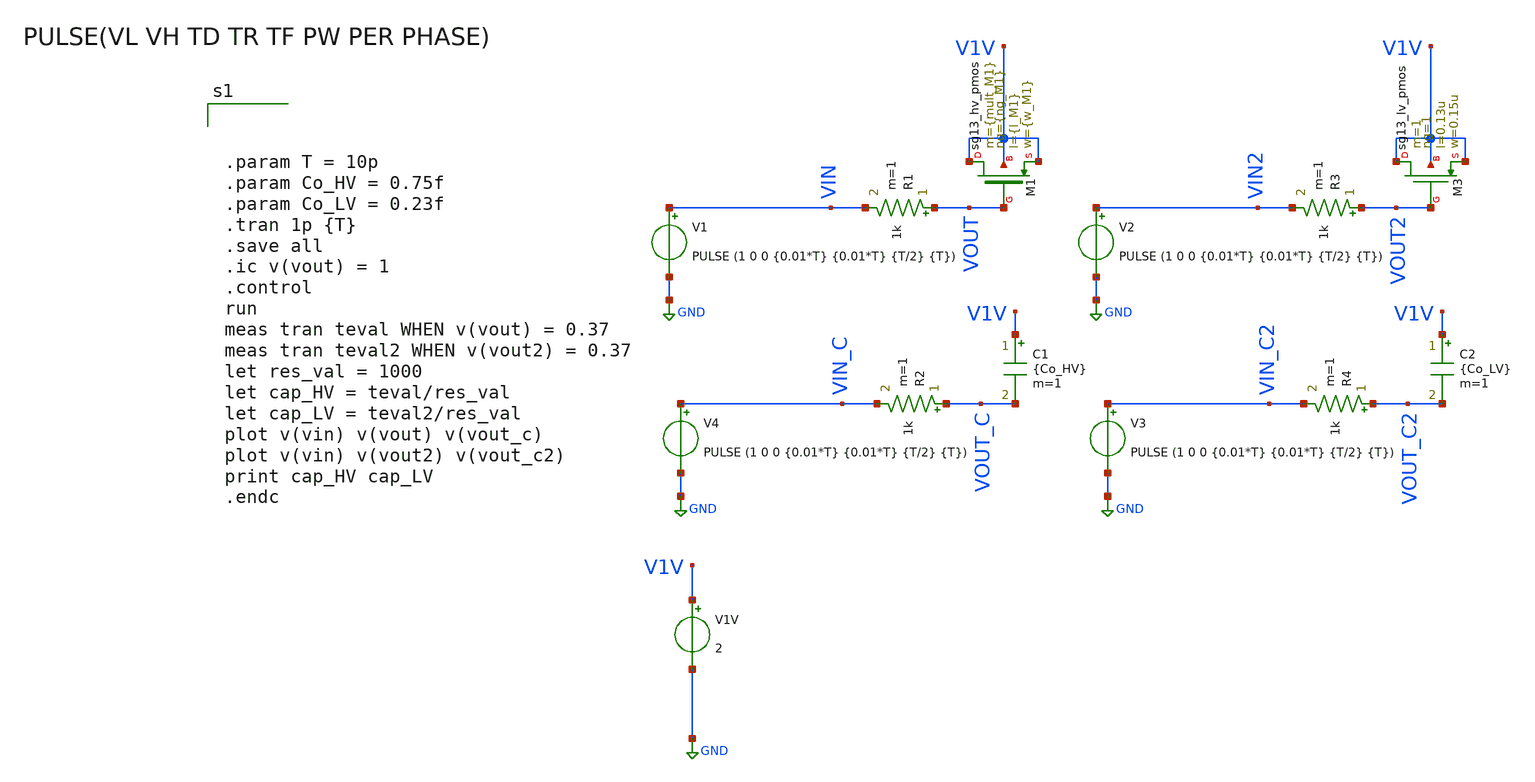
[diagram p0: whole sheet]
** sch_path: xschem/DCDCBuck/TB_hvPMOS_cgate_ext.sch
**.subckt TB_hvPMOS_cgate_ext
R1 VOUT VIN 1k m=1
V1 VIN GND PULSE (1 0 0 {0.01*T} {0.01*T} {T/2} {T})
V1V V1V GND 2
R2 VOUT_C VIN_C 1k m=1
C1 V1V VOUT_C {Co_HV} m=1
XM1 V1V VOUT V1V V1V sg13_hv_pmos w={w_M1} l={l_M1} ng={ng_M1} m={mult_M1} mm_ok=1
R3 VOUT2 VIN2 1k m=1
R4 VOUT_C2 VIN_C2 1k m=1
C2 V1V VOUT_C2 {Co_LV} m=1
XM3 V1V VOUT2 V1V V1V sg13_lv_pmos w=0.15u l=0.13u ng=1 m=1 mm_ok=1
V2 VIN2 GND PULSE (1 0 0 {0.01*T} {0.01*T} {T/2} {T})
V3 VIN_C2 GND PULSE (1 0 0 {0.01*T} {0.01*T} {T/2} {T})
V4 VIN_C GND PULSE (1 0 0 {0.01*T} {0.01*T} {T/2} {T})
**** begin user architecture code



.param T = 10p
.param Co_HV = 0.75f
.param Co_LV = 0.23f
.tran 1p {T}
.save all
.ic v(vout) = 1
.control
run
meas tran teval WHEN v(vout) = 0.37
meas tran teval2 WHEN v(vout2) = 0.37
let res_val = 1000
let cap_HV = teval/res_val
let cap_LV = teval2/res_val
plot v(vin) v(vout) v(vout_c)
plot v(vin) v(vout2) v(vout_c2)
print cap_HV cap_LV
.endc




.lib cornerMOShv.lib mos_tt
.lib cornerMOSlv.lib mos_tt
*.lib cornerMOShv.lib mos_ff
*.lib cornerMOSlv.lib mos_ff
*.lib cornerMOShv.lib mos_ss
*.lib cornerMOSlv.lib mos_ss
*.lib cornerMOShv.lib mos_sf
*.lib cornerMOSlv.lib mos_sf
*.lib cornerMOShv.lib mos_fs
*.lib cornerMOSlv.lib mos_fs

.include /opt/pdks/ihp-sg13g2/libs.ref/sg13g2_stdcell/spice/sg13g2_stdcell.spice
.lib $::SG13G2_MODELS/cornerRES.lib res_typ
.lib $::SG13G2_MODELS/cornerCAP.lib cap_typ
*.lib $::SG13G2_MODELS/diodes.lib



.param mult = 1
.param temp=27
.param mult_M1 = 1*mult
.param w_M1 =0.3u
.param l_M1 = 0.45u
.param ng_M1 = 1

.param mult_M2 = 1*mult
.param w_M2 =0.3u
.param l_M2 =0.45u
.param ng_M2 =1





**** end user architecture code
**.ends
.GLOBAL GND
.end
